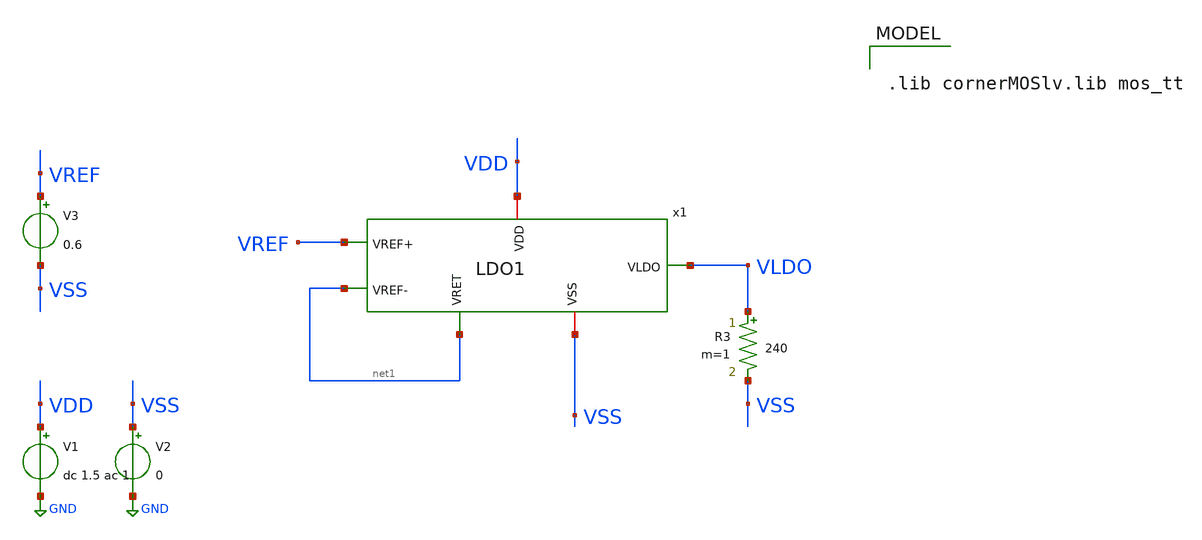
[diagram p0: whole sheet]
** sch_path: designs/1iee34/tb_ldo_noise_2.sch
**.subckt tb_ldo_noise_2
V1 VDD GND dc 1.5 ac 1
V2 VSS GND 0
V3 VREF VSS 0.6
R3 VLDO VSS 240 m=1
x1 VDD VREF net1 VLDO net1 VSS LDO1
**** begin user architecture code


.param temp=27
.options savecurrents
.op
.save all  @n.x1.xmG.nsg13_lv_pmos[ids]  @n.x1.xmG.nsg13_lv_pmos[gm]  @n.x1.xmG.nsg13_lv_pmos[gds]  @n.x1.xm6.nsg13_lv_pmos[gds]  @n.x1.xm6.nsg13_lv_pmos[gm]  @n.x1.xm5.nsg13_lv_nmos[ids]  @n.x1.xm5.nsg13_lv_nmos[gm]  @n.x1.xm5.nsg13_lv_nmos[gds]  @n.x1.xm8.nsg13_lv_nmos[ids]  @n.x1.xm7.nsg13_lv_nmos[ids]  @n.x1.xm7.nsg13_lv_nmos[gm]  @n.x1.xm7.nsg13_lv_nmos[gds]

.control
  noise v(vldo) v1 dec 80 1 10000k 1
  print inoise_total onoise_total
  set filetype = ascii
  write ckt_noise2_all.raw noise1.all noise2.all
  setplot noise1
  write ckt_noise2_1.raw all
  write ckt_noise2.raw inoise_spectrum onoise_spectrum
  setplot noise2
  write ckt_noise2_2.raw all
.endc




.lib cornerMOSlv.lib mos_tt


**** end user architecture code
**.ends

* expanding   symbol:  LDO1.sym # of pins=6
** sym_path: designs/1iee34/LDO1.sym
** sch_path: designs/1iee34/LDO1.sch
.subckt LDO1 VDD VREF+ VREF- VLDO VRET VSS
*.iopin VREF+
*.iopin VLDO
*.iopin VDD
*.iopin VREF-
*.iopin VSS
*.iopin VRET
C1 VLDO VSS 1000.0n m=1
CC net4 net1 3.666349378452877e-05n m=1
R1 VLDO VRET 21.49k m=1
R2 VRET VSS 21.49k m=1
C3 VLDO net5 5n m=1
R3 net1 net5 30k m=1
XMG VLDO net1 VDD VDD sg13_lv_pmos w=250.0u l=0.13u ng=13 m=1 mm_ok=1
XM3 net3 net3 VDD VDD sg13_lv_pmos w=14.74u l=32.58u ng=2 m=1 mm_ok=1
XM4 net4 net3 VDD VDD sg13_lv_pmos w=14.74u l=32.58u ng=2 m=1 mm_ok=1
XM6 net1 net4 VDD VDD sg13_lv_pmos w=3.58u l=1.5u ng=1 m=1 mm_ok=1
XM1 net2 VREF+ net3 VSS sg13_lv_nmos w=176.34u l=8.55u ng=18 m=1 mm_ok=1
XM2 net2 VREF- net4 VSS sg13_lv_nmos w=176.34u l=8.55u ng=18 m=1 mm_ok=1
XM5 VSS VG net2 VSS sg13_lv_nmos w=2.2u l=2.0u ng=1 m=1 mm_ok=1
XM7 VSS VG net1 VSS sg13_lv_nmos w=4.4u l=2.0u ng=1 m=1 mm_ok=1
XM8 VSS VG VG VSS sg13_lv_nmos w=2.75u l=2.0u ng=1 m=1 mm_ok=1
XM10 net6 net6 VDD VDD sg13_lv_pmos w=2u l=8u ng=1 m=1 mm_ok=1
XM11 VG VDD net6 VSS sg13_lv_nmos w=2u l=8u ng=1 m=1 mm_ok=1
.ends

.GLOBAL GND
.end
